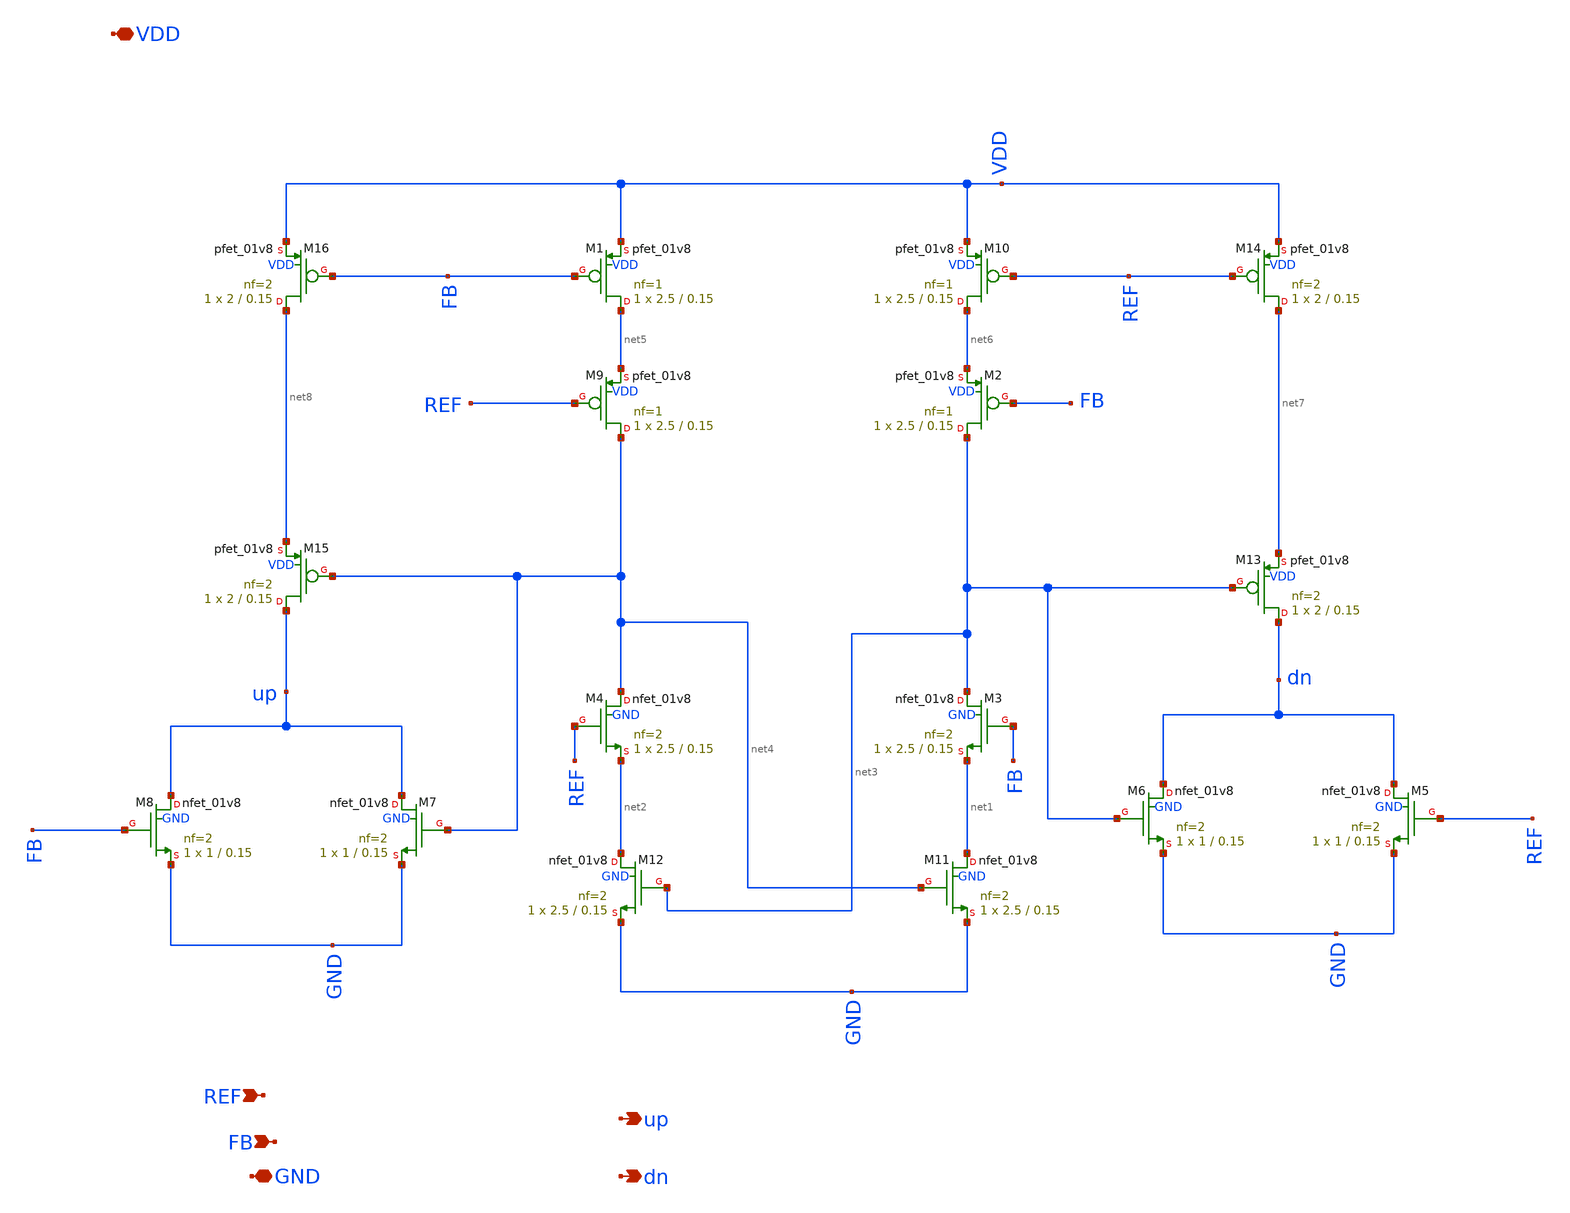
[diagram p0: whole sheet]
** sch_path: pll/pfd_cp_lf_lib/PFD+CP_tb/xschem/PFD.sch
**.subckt PFD VDD GND REF FB up dn
*.iopin VDD
*.iopin GND
*.ipin REF
*.ipin FB
*.opin up
*.opin dn
XM3 net3 FB net1 GND sky130_fd_pr__nfet_01v8 L=0.15 W=2.5 nf=2 ad='int((nf+1)/2) * W/nf * 0.29' as='int((nf+2)/2) * W/nf * 0.29'
+ pd='2*int((nf+1)/2) * (W/nf + 0.29)' ps='2*int((nf+2)/2) * (W/nf + 0.29)' nrd='0.29 / W' nrs='0.29 / W'
+ sa=0 sb=0 sd=0 mult=1 m=1
XM4 net4 REF net2 GND sky130_fd_pr__nfet_01v8 L=0.15 W=2.5 nf=2 ad='int((nf+1)/2) * W/nf * 0.29' as='int((nf+2)/2) * W/nf * 0.29'
+ pd='2*int((nf+1)/2) * (W/nf + 0.29)' ps='2*int((nf+2)/2) * (W/nf + 0.29)' nrd='0.29 / W' nrs='0.29 / W'
+ sa=0 sb=0 sd=0 mult=1 m=1
XM5 dn REF GND GND sky130_fd_pr__nfet_01v8 L=0.15 W=1 nf=2 ad='int((nf+1)/2) * W/nf * 0.29' as='int((nf+2)/2) * W/nf * 0.29'
+ pd='2*int((nf+1)/2) * (W/nf + 0.29)' ps='2*int((nf+2)/2) * (W/nf + 0.29)' nrd='0.29 / W' nrs='0.29 / W'
+ sa=0 sb=0 sd=0 mult=1 m=1
XM6 dn net3 GND GND sky130_fd_pr__nfet_01v8 L=0.15 W=1 nf=2 ad='int((nf+1)/2) * W/nf * 0.29' as='int((nf+2)/2) * W/nf * 0.29'
+ pd='2*int((nf+1)/2) * (W/nf + 0.29)' ps='2*int((nf+2)/2) * (W/nf + 0.29)' nrd='0.29 / W' nrs='0.29 / W'
+ sa=0 sb=0 sd=0 mult=1 m=1
XM7 up net4 GND GND sky130_fd_pr__nfet_01v8 L=0.15 W=1 nf=2 ad='int((nf+1)/2) * W/nf * 0.29' as='int((nf+2)/2) * W/nf * 0.29'
+ pd='2*int((nf+1)/2) * (W/nf + 0.29)' ps='2*int((nf+2)/2) * (W/nf + 0.29)' nrd='0.29 / W' nrs='0.29 / W'
+ sa=0 sb=0 sd=0 mult=1 m=1
XM8 up FB GND GND sky130_fd_pr__nfet_01v8 L=0.15 W=1 nf=2 ad='int((nf+1)/2) * W/nf * 0.29' as='int((nf+2)/2) * W/nf * 0.29'
+ pd='2*int((nf+1)/2) * (W/nf + 0.29)' ps='2*int((nf+2)/2) * (W/nf + 0.29)' nrd='0.29 / W' nrs='0.29 / W'
+ sa=0 sb=0 sd=0 mult=1 m=1
XM9 net4 REF net5 VDD sky130_fd_pr__pfet_01v8 L=0.15 W=2.5 nf=1 ad='int((nf+1)/2) * W/nf * 0.29' as='int((nf+2)/2) * W/nf * 0.29'
+ pd='2*int((nf+1)/2) * (W/nf + 0.29)' ps='2*int((nf+2)/2) * (W/nf + 0.29)' nrd='0.29 / W' nrs='0.29 / W'
+ sa=0 sb=0 sd=0 mult=1 m=1
XM1 net5 FB VDD VDD sky130_fd_pr__pfet_01v8 L=0.15 W=2.5 nf=1 ad='int((nf+1)/2) * W/nf * 0.29' as='int((nf+2)/2) * W/nf * 0.29'
+ pd='2*int((nf+1)/2) * (W/nf + 0.29)' ps='2*int((nf+2)/2) * (W/nf + 0.29)' nrd='0.29 / W' nrs='0.29 / W'
+ sa=0 sb=0 sd=0 mult=1 m=1
XM2 net3 FB net6 VDD sky130_fd_pr__pfet_01v8 L=0.15 W=2.5 nf=1 ad='int((nf+1)/2) * W/nf * 0.29' as='int((nf+2)/2) * W/nf * 0.29'
+ pd='2*int((nf+1)/2) * (W/nf + 0.29)' ps='2*int((nf+2)/2) * (W/nf + 0.29)' nrd='0.29 / W' nrs='0.29 / W'
+ sa=0 sb=0 sd=0 mult=1 m=1
XM10 net6 REF VDD VDD sky130_fd_pr__pfet_01v8 L=0.15 W=2.5 nf=1 ad='int((nf+1)/2) * W/nf * 0.29' as='int((nf+2)/2) * W/nf * 0.29'
+ pd='2*int((nf+1)/2) * (W/nf + 0.29)' ps='2*int((nf+2)/2) * (W/nf + 0.29)' nrd='0.29 / W' nrs='0.29 / W'
+ sa=0 sb=0 sd=0 mult=1 m=1
XM13 dn net3 net7 VDD sky130_fd_pr__pfet_01v8 L=0.15 W=2 nf=2 ad='int((nf+1)/2) * W/nf * 0.29' as='int((nf+2)/2) * W/nf * 0.29'
+ pd='2*int((nf+1)/2) * (W/nf + 0.29)' ps='2*int((nf+2)/2) * (W/nf + 0.29)' nrd='0.29 / W' nrs='0.29 / W'
+ sa=0 sb=0 sd=0 mult=1 m=1
XM14 net7 REF VDD VDD sky130_fd_pr__pfet_01v8 L=0.15 W=2 nf=2 ad='int((nf+1)/2) * W/nf * 0.29' as='int((nf+2)/2) * W/nf * 0.29'
+ pd='2*int((nf+1)/2) * (W/nf + 0.29)' ps='2*int((nf+2)/2) * (W/nf + 0.29)' nrd='0.29 / W' nrs='0.29 / W'
+ sa=0 sb=0 sd=0 mult=1 m=1
XM15 up net4 net8 VDD sky130_fd_pr__pfet_01v8 L=0.15 W=2 nf=2 ad='int((nf+1)/2) * W/nf * 0.29' as='int((nf+2)/2) * W/nf * 0.29'
+ pd='2*int((nf+1)/2) * (W/nf + 0.29)' ps='2*int((nf+2)/2) * (W/nf + 0.29)' nrd='0.29 / W' nrs='0.29 / W'
+ sa=0 sb=0 sd=0 mult=1 m=1
XM16 net8 FB VDD VDD sky130_fd_pr__pfet_01v8 L=0.15 W=2 nf=2 ad='int((nf+1)/2) * W/nf * 0.29' as='int((nf+2)/2) * W/nf * 0.29'
+ pd='2*int((nf+1)/2) * (W/nf + 0.29)' ps='2*int((nf+2)/2) * (W/nf + 0.29)' nrd='0.29 / W' nrs='0.29 / W'
+ sa=0 sb=0 sd=0 mult=1 m=1
XM11 net1 net4 GND GND sky130_fd_pr__nfet_01v8 L=0.15 W=2.5 nf=2 ad='int((nf+1)/2) * W/nf * 0.29' as='int((nf+2)/2) * W/nf * 0.29'
+ pd='2*int((nf+1)/2) * (W/nf + 0.29)' ps='2*int((nf+2)/2) * (W/nf + 0.29)' nrd='0.29 / W' nrs='0.29 / W'
+ sa=0 sb=0 sd=0 mult=1 m=1
XM12 net2 net3 GND GND sky130_fd_pr__nfet_01v8 L=0.15 W=2.5 nf=2 ad='int((nf+1)/2) * W/nf * 0.29' as='int((nf+2)/2) * W/nf * 0.29'
+ pd='2*int((nf+1)/2) * (W/nf + 0.29)' ps='2*int((nf+2)/2) * (W/nf + 0.29)' nrd='0.29 / W' nrs='0.29 / W'
+ sa=0 sb=0 sd=0 mult=1 m=1
**.ends
.end
